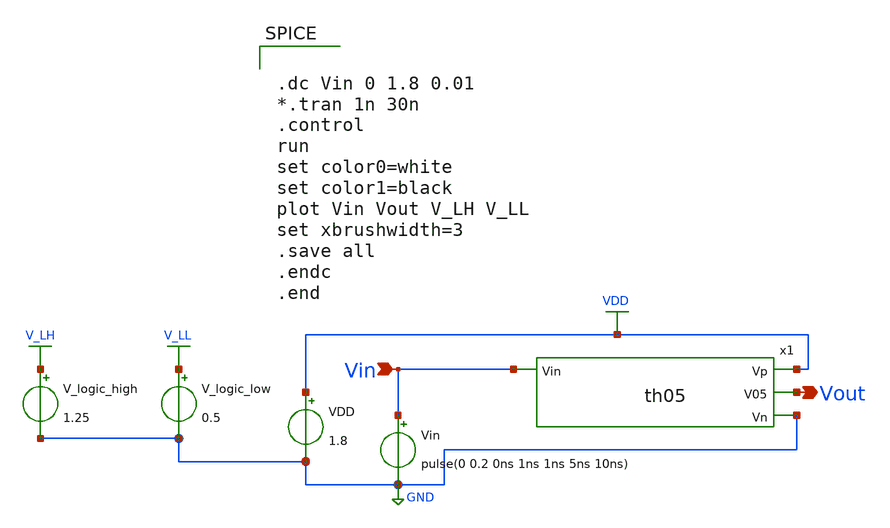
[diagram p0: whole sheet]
** sch_path: xschem/Vth_sch/Pre_layout/th05.sch
**.subckt th05 Vin Vout
*.ipin Vin
*.opin Vout
VDD VDD GND 1.8
Vin Vin GND pulse(0 0.2 0ns 1ns 1ns 5ns 10ns)
V_logic_high V_LH GND 1.25
V_logic_low V_LL GND 0.5
x1 VDD Vout Vin GND th05
**** begin user architecture code


.lib /usr/local/share/pdk/sky130A/libs.tech/ngspice/sky130.lib.spice tt

.save all





.dc Vin 0 1.8 0.01
*.tran 1n 30n
.control
run
set color0=white
set color1=black
plot Vin Vout V_LH V_LL
set xbrushwidth=3
.save all
.endc
.end


**** end user architecture code
**.ends

* expanding   symbol:  /home/exotic/Desktop/ASIC_ADC/xschem/Vth_sch/Symbol/th05.sym # of pins=4
** sym_path: xschem/Vth_sch/Symbol/th05.sym
** sch_path: xschem/Vth_sch/Symbol/th05.sch
.subckt th05 Vp V05 Vin Vn
*.opin Vn
*.opin Vp
*.ipin Vin
*.opin V05
XM2 V05 net1 Vp Vp sky130_fd_pr__pfet_01v8 L=1.12 W=0.5 nf=1 ad='int((nf+1)/2) * W/nf * 0.29' as='int((nf+2)/2) * W/nf * 0.29'
+ pd='2*int((nf+1)/2) * (W/nf + 0.29)' ps='2*int((nf+2)/2) * (W/nf + 0.29)' nrd='0.29 / W' nrs='0.29 / W'
+ sa=0 sb=0 sd=0 mult=1 m=1
XM3 V05 net1 Vn Vn sky130_fd_pr__nfet_01v8 L=0.18 W=1.0 nf=1 ad='int((nf+1)/2) * W/nf * 0.29' as='int((nf+2)/2) * W/nf * 0.29'
+ pd='2*int((nf+1)/2) * (W/nf + 0.29)' ps='2*int((nf+2)/2) * (W/nf + 0.29)' nrd='0.29 / W' nrs='0.29 / W'
+ sa=0 sb=0 sd=0 mult=1 m=1
XM1 net1 Vin Vp Vp sky130_fd_pr__pfet_01v8 L=1.633 W=0.42 nf=1 ad='int((nf+1)/2) * W/nf * 0.29' as='int((nf+2)/2) * W/nf * 0.29'
+ pd='2*int((nf+1)/2) * (W/nf + 0.29)' ps='2*int((nf+2)/2) * (W/nf + 0.29)' nrd='0.29 / W' nrs='0.29 / W'
+ sa=0 sb=0 sd=0 mult=1 m=1
XM0 net1 Vin Vn Vn sky130_fd_pr__nfet_01v8 L=0.2 W=2.00 nf=1 ad='int((nf+1)/2) * W/nf * 0.29' as='int((nf+2)/2) * W/nf * 0.29'
+ pd='2*int((nf+1)/2) * (W/nf + 0.29)' ps='2*int((nf+2)/2) * (W/nf + 0.29)' nrd='0.29 / W' nrs='0.29 / W'
+ sa=0 sb=0 sd=0 mult=1 m=1
.ends

.GLOBAL VDD
.GLOBAL GND
.GLOBAL V_LH
.GLOBAL V_LL
.end
